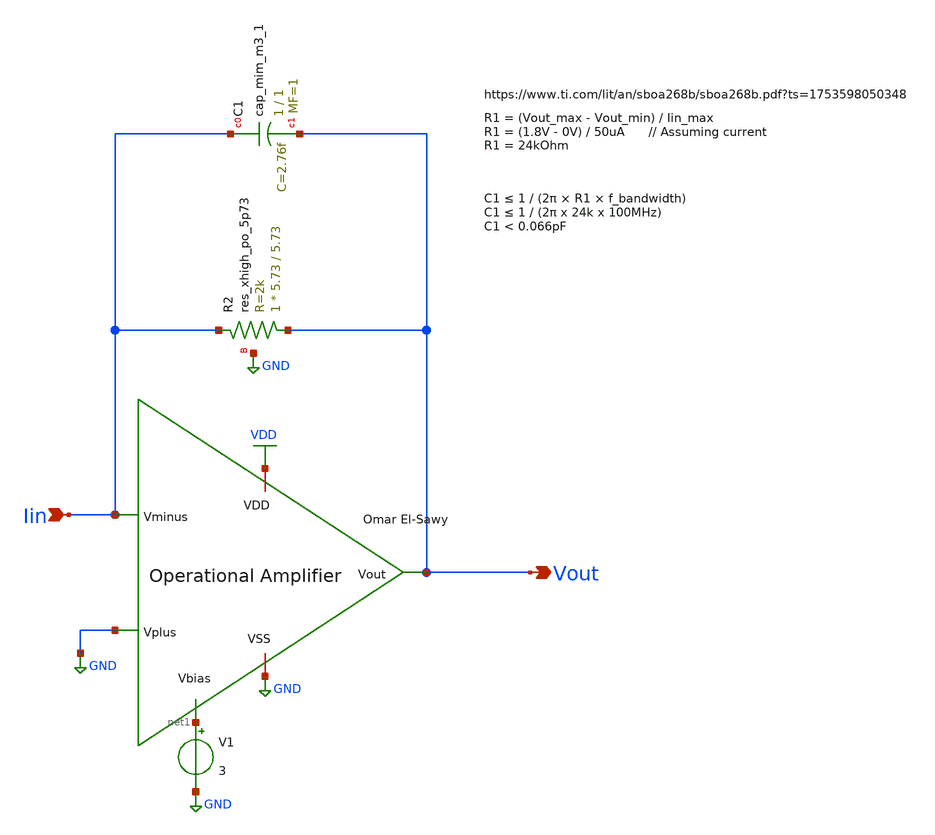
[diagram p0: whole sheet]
** sch_path: analog/schematics/CurrentSensor.sch
**.subckt CurrentSensor Iin Vout
*.ipin Iin
*.opin Vout
x1 VDD Vout Iin GND net1 GND OpAmp
V1 net1 GND 3
XC1 Iin Vout sky130_fd_pr__cap_mim_m3_1 W=1 L=1 MF=1 m=1
XR2 Vout Iin GND sky130_fd_pr__res_xhigh_po_5p73 L=5.73 mult=1 m=1
**.ends

* expanding   symbol:  Operational_Amplifiers/OpAmp.sym # of pins=6
** sym_path: Operational_Amplifiers/OpAmp.sym
** sch_path: Operational_Amplifiers/OpAmp.sch
.subckt OpAmp VDD Vout Vminus Vplus Vbias VSS
*.ipin Vbias
*.ipin Vplus
*.ipin Vminus
*.opin Vout
*.iopin VDD
*.iopin VSS
XM1 net2 Vminus net1 VSS sky130_fd_pr__nfet_01v8 L=0.15 W=10 nf=1 ad='int((nf+1)/2) * W/nf * 0.29' as='int((nf+2)/2) * W/nf * 0.29'
+ pd='2*int((nf+1)/2) * (W/nf + 0.29)' ps='2*int((nf+2)/2) * (W/nf + 0.29)' nrd='0.29 / W' nrs='0.29 / W'
+ sa=0 sb=0 sd=0 mult=1 m=1
XM2 V1st Vplus net1 VSS sky130_fd_pr__nfet_01v8 L=0.15 W=10 nf=1 ad='int((nf+1)/2) * W/nf * 0.29' as='int((nf+2)/2) * W/nf * 0.29'
+ pd='2*int((nf+1)/2) * (W/nf + 0.29)' ps='2*int((nf+2)/2) * (W/nf + 0.29)' nrd='0.29 / W' nrs='0.29 / W'
+ sa=0 sb=0 sd=0 mult=1 m=1
XM3 net1 Vbias VSS VSS sky130_fd_pr__nfet_01v8 L=0.3 W=15 nf=1 ad='int((nf+1)/2) * W/nf * 0.29' as='int((nf+2)/2) * W/nf * 0.29'
+ pd='2*int((nf+1)/2) * (W/nf + 0.29)' ps='2*int((nf+2)/2) * (W/nf + 0.29)' nrd='0.29 / W' nrs='0.29 / W'
+ sa=0 sb=0 sd=0 mult=1 m=1
XM4 net2 net2 VDD VDD sky130_fd_pr__pfet_01v8 L=0.15 W=5 nf=1 ad='int((nf+1)/2) * W/nf * 0.29' as='int((nf+2)/2) * W/nf * 0.29'
+ pd='2*int((nf+1)/2) * (W/nf + 0.29)' ps='2*int((nf+2)/2) * (W/nf + 0.29)' nrd='0.29 / W' nrs='0.29 / W'
+ sa=0 sb=0 sd=0 mult=1 m=1
XM5 V1st net2 VDD VDD sky130_fd_pr__pfet_01v8 L=0.15 W=5 nf=1 ad='int((nf+1)/2) * W/nf * 0.29' as='int((nf+2)/2) * W/nf * 0.29'
+ pd='2*int((nf+1)/2) * (W/nf + 0.29)' ps='2*int((nf+2)/2) * (W/nf + 0.29)' nrd='0.29 / W' nrs='0.29 / W'
+ sa=0 sb=0 sd=0 mult=1 m=1
XM6 Vout V1st VDD VDD sky130_fd_pr__pfet_01v8 L=0.15 W=20 nf=1 ad='int((nf+1)/2) * W/nf * 0.29' as='int((nf+2)/2) * W/nf * 0.29'
+ pd='2*int((nf+1)/2) * (W/nf + 0.29)' ps='2*int((nf+2)/2) * (W/nf + 0.29)' nrd='0.29 / W' nrs='0.29 / W'
+ sa=0 sb=0 sd=0 mult=1 m=1
XM7 Vout Vbias VSS VSS sky130_fd_pr__nfet_01v8 L=0.15 W=10 nf=1 ad='int((nf+1)/2) * W/nf * 0.29' as='int((nf+2)/2) * W/nf * 0.29'
+ pd='2*int((nf+1)/2) * (W/nf + 0.29)' ps='2*int((nf+2)/2) * (W/nf + 0.29)' nrd='0.29 / W' nrs='0.29 / W'
+ sa=0 sb=0 sd=0 mult=1 m=1
XC2 Vout V1st sky130_fd_pr__cap_mim_m3_2 W=12 L=1 MF=12 m=12
.ends

.GLOBAL VDD
.GLOBAL GND
.GLOBAL VSS
.end
